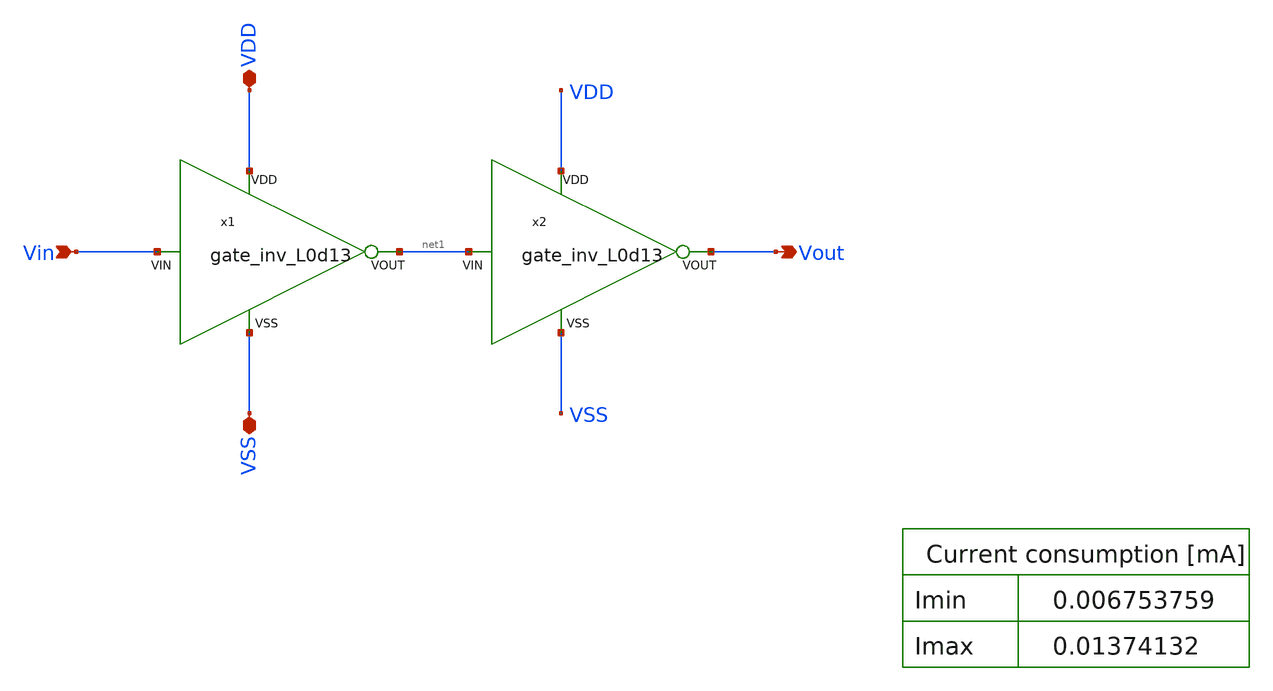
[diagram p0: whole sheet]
** sch_path: work/comparator_inv/xschem/comparator_inv.sch
**.subckt comparator_inv VDD VSS Vin Vout
*.iopin VDD
*.iopin VSS
*.ipin Vin
*.opin Vout
x1 VDD Vin net1 VSS gate_inv_L0d13
x2 VDD net1 Vout VSS gate_inv_L0d13
**.ends

* expanding   symbol:
*+  /foss/designs/chipathon_2025/designs/ihp-sg13g2/gate_inv_L0d13/xschem/gate_inv_L0d13.sym # of pins=4
** sym_path: /foss/designs/chipathon_2025/designs/ihp-sg13g2/gate_inv_L0d13/xschem/gate_inv_L0d13.sym
** sch_path: /foss/designs/chipathon_2025/designs/ihp-sg13g2/gate_inv_L0d13/xschem/gate_inv_L0d13.sch
.subckt gate_inv_L0d13 VDD VIN VOUT VSS
*.ipin VDD
*.ipin VSS
*.ipin VIN
*.opin VOUT
XM2 VDD VIN VOUT VDD sg13_lv_pmos w=2u l=0.13u ng=1 m=1 mm_ok=1
XM1 VOUT VIN VSS VSS sg13_lv_nmos w=1.0u l=0.13u ng=1 m=1 mm_ok=1
.ends

.end
